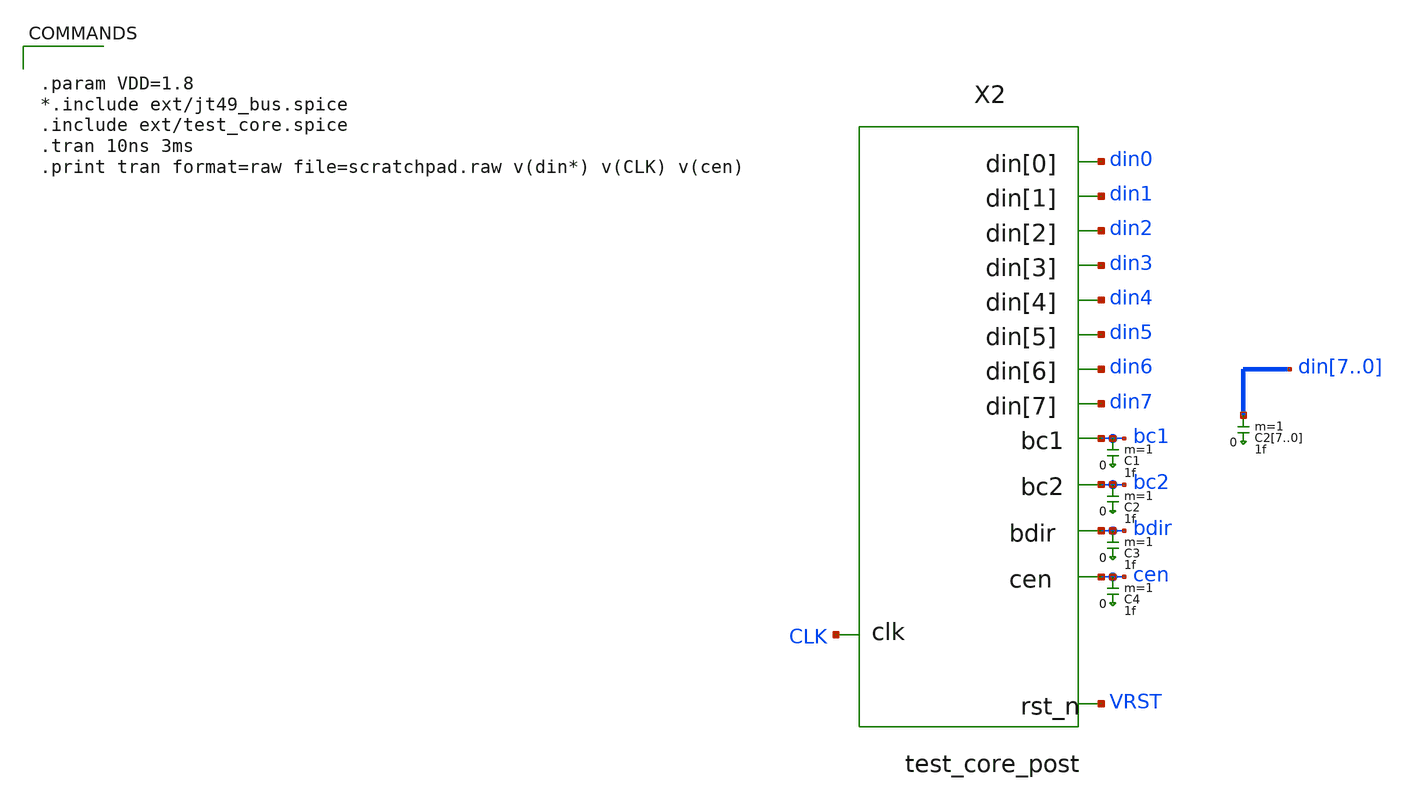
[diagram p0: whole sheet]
** sch_path: xschem/scratchpad.sch
**.subckt scratchpad
X2 CLK cen VRST bdir bc1 bc2 din7 din6 din5 din4 din3 din2 din1 din0 test_core
C27 din7 0 1f m=1
C26 din6 0 1f m=1
C25 din5 0 1f m=1
C24 din4 0 1f m=1
C23 din3 0 1f m=1
C22 din2 0 1f m=1
C21 din1 0 1f m=1
C20 din0 0 1f m=1
C1 bc1 0 1f m=1
C2 bc2 0 1f m=1
C3 bdir 0 1f m=1
C4 cen 0 1f m=1
**** begin user architecture code


.param VDD=1.8
*.include ext/jt49_bus.spice
.include ext/test_core.spice
.tran 10ns 3ms
.print tran format=raw file=scratchpad.raw v(din*) v(CLK) v(cen)


**** end user architecture code
**.ends
.end
